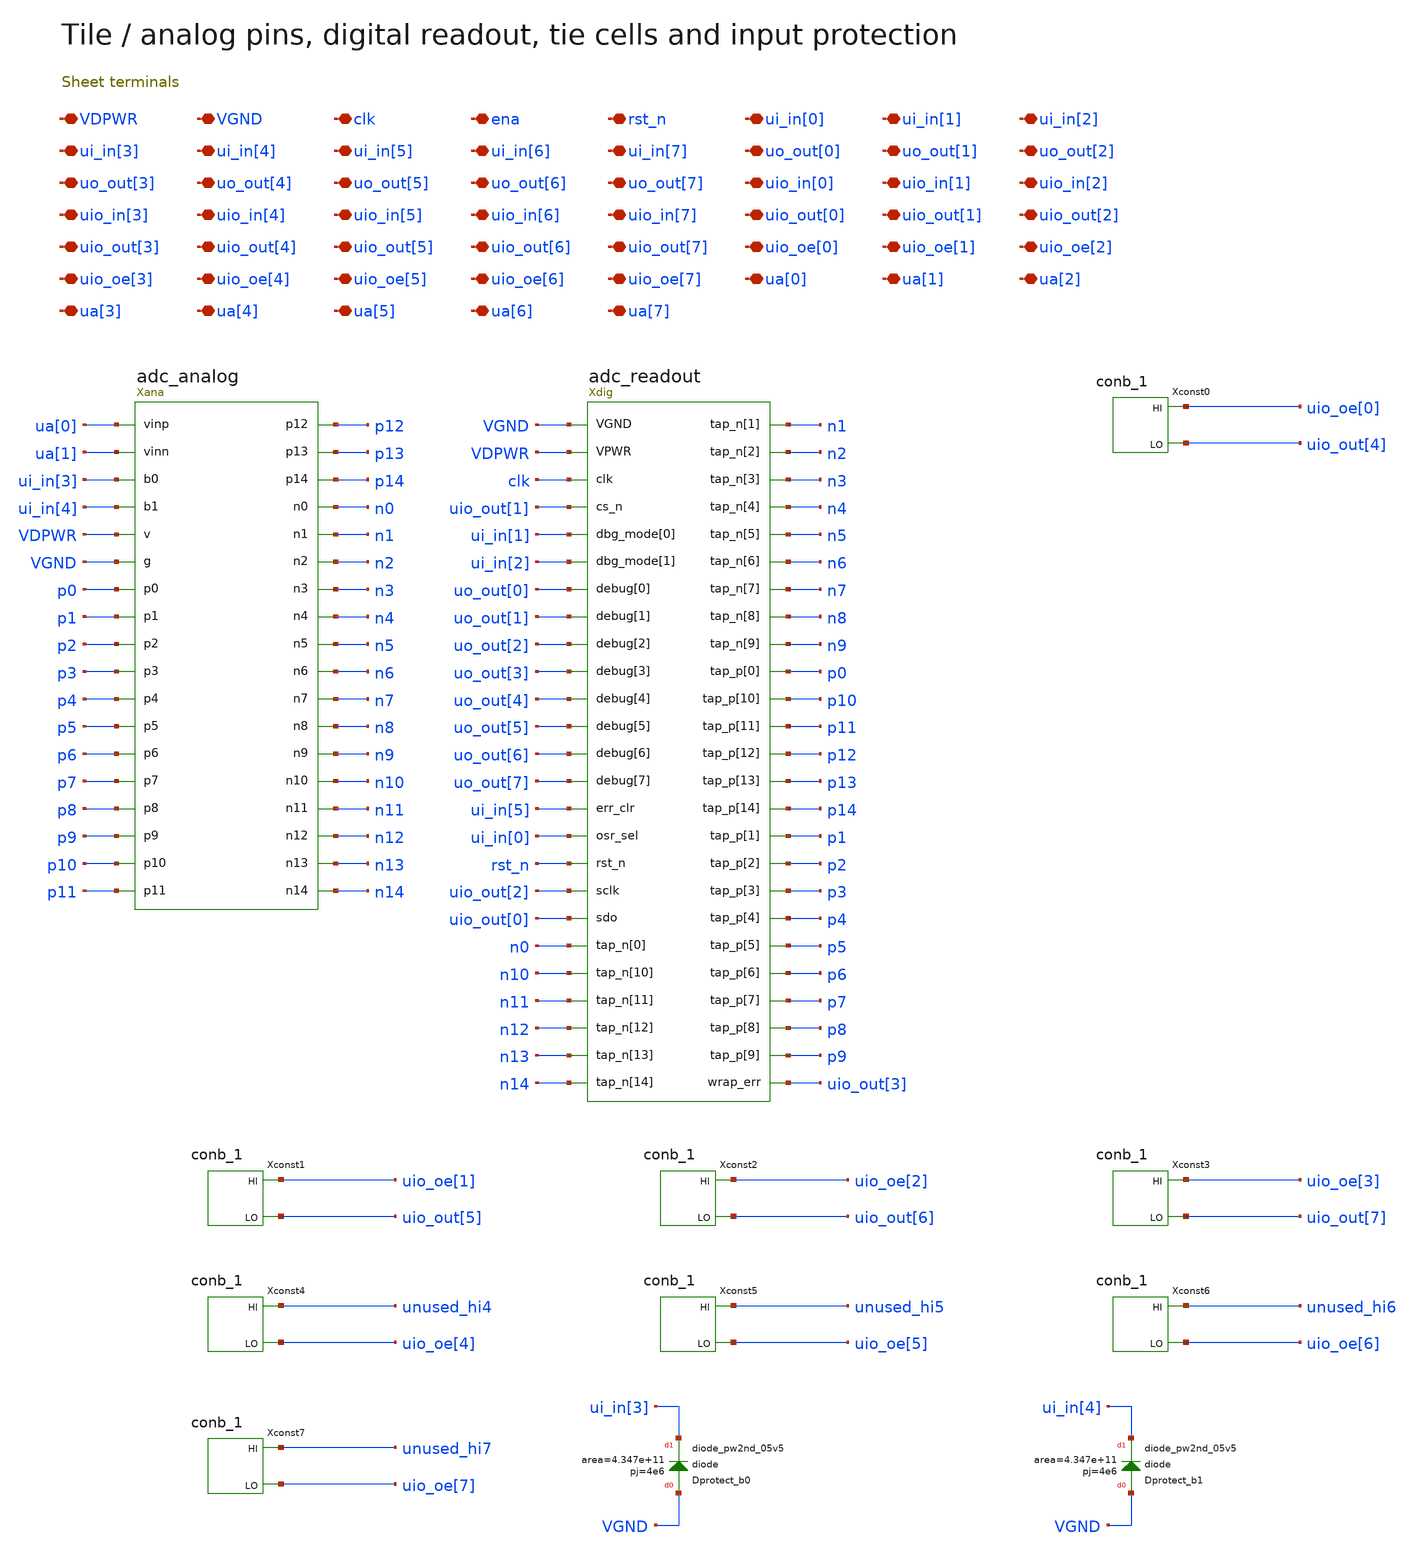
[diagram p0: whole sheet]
** sch_path: review/xschem/tt_um_eleva_ccro_adc.sch
**.subckt tt_um_eleva_ccro_adc VDPWR VGND clk ena rst_n ui_in[0] ui_in[1] ui_in[2] ui_in[3] ui_in[4]
*+ ui_in[5] ui_in[6] ui_in[7] uo_out[0] uo_out[1] uo_out[2] uo_out[3] uo_out[4] uo_out[5] uo_out[6] uo_out[7]
*+ uio_in[0] uio_in[1] uio_in[2] uio_in[3] uio_in[4] uio_in[5] uio_in[6] uio_in[7] uio_out[0] uio_out[1]
*+ uio_out[2] uio_out[3] uio_out[4] uio_out[5] uio_out[6] uio_out[7] uio_oe[0] uio_oe[1] uio_oe[2] uio_oe[3]
*+ uio_oe[4] uio_oe[5] uio_oe[6] uio_oe[7] ua[0] ua[1] ua[2] ua[3] ua[4] ua[5] ua[6] ua[7]
*.iopin VDPWR
*.iopin VGND
*.iopin clk
*.iopin ena
*.iopin rst_n
*.iopin ui_in[0]
*.iopin ui_in[1]
*.iopin ui_in[2]
*.iopin ui_in[3]
*.iopin ui_in[4]
*.iopin ui_in[5]
*.iopin ui_in[6]
*.iopin ui_in[7]
*.iopin uo_out[0]
*.iopin uo_out[1]
*.iopin uo_out[2]
*.iopin uo_out[3]
*.iopin uo_out[4]
*.iopin uo_out[5]
*.iopin uo_out[6]
*.iopin uo_out[7]
*.iopin uio_in[0]
*.iopin uio_in[1]
*.iopin uio_in[2]
*.iopin uio_in[3]
*.iopin uio_in[4]
*.iopin uio_in[5]
*.iopin uio_in[6]
*.iopin uio_in[7]
*.iopin uio_out[0]
*.iopin uio_out[1]
*.iopin uio_out[2]
*.iopin uio_out[3]
*.iopin uio_out[4]
*.iopin uio_out[5]
*.iopin uio_out[6]
*.iopin uio_out[7]
*.iopin uio_oe[0]
*.iopin uio_oe[1]
*.iopin uio_oe[2]
*.iopin uio_oe[3]
*.iopin uio_oe[4]
*.iopin uio_oe[5]
*.iopin uio_oe[6]
*.iopin uio_oe[7]
*.iopin ua[0]
*.iopin ua[1]
*.iopin ua[2]
*.iopin ua[3]
*.iopin ua[4]
*.iopin ua[5]
*.iopin ua[6]
*.iopin ua[7]
Xana ua[0] ua[1] ui_in[3] ui_in[4] VDPWR VGND p0 p1 p2 p3 p4 p5 p6 p7 p8 p9 p10 p11 p12 p13 p14 n0
+ n1 n2 n3 n4 n5 n6 n7 n8 n9 n10 n11 n12 n13 n14 adc_analog
Xdig VGND VDPWR clk uio_out[1] ui_in[1] ui_in[2] uo_out[0] uo_out[1] uo_out[2] uo_out[3] uo_out[4]
+ uo_out[5] uo_out[6] uo_out[7] ui_in[5] ui_in[0] rst_n uio_out[2] uio_out[0] n0 n10 n11 n12 n13 n14 n1 n2 n3
+ n4 n5 n6 n7 n8 n9 p0 p10 p11 p12 p13 p14 p1 p2 p3 p4 p5 p6 p7 p8 p9 uio_out[3] adc_readout
Xconst0 VGND VGND VDPWR VDPWR uio_oe[0] uio_out[4] sky130_fd_sc_hd__conb_1
Xconst1 VGND VGND VDPWR VDPWR uio_oe[1] uio_out[5] sky130_fd_sc_hd__conb_1
Xconst2 VGND VGND VDPWR VDPWR uio_oe[2] uio_out[6] sky130_fd_sc_hd__conb_1
Xconst3 VGND VGND VDPWR VDPWR uio_oe[3] uio_out[7] sky130_fd_sc_hd__conb_1
Xconst4 VGND VGND VDPWR VDPWR unused_hi4 uio_oe[4] sky130_fd_sc_hd__conb_1
Xconst5 VGND VGND VDPWR VDPWR unused_hi5 uio_oe[5] sky130_fd_sc_hd__conb_1
Xconst6 VGND VGND VDPWR VDPWR unused_hi6 uio_oe[6] sky130_fd_sc_hd__conb_1
Xconst7 VGND VGND VDPWR VDPWR unused_hi7 uio_oe[7] sky130_fd_sc_hd__conb_1
XDprotect_b0 VGND ui_in[3] sky130_fd_pr__diode_pw2nd_05v5 area=4.347e+11 pj=4e6
XDprotect_b1 VGND ui_in[4] sky130_fd_pr__diode_pw2nd_05v5 area=4.347e+11 pj=4e6
**.ends
.end
